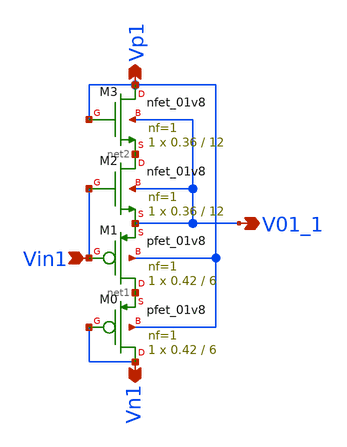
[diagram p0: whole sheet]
** sch_path: xschem/Vth_sch/Symbol/th01_1.sch
**.subckt th01_1 Vn1 Vp1 Vin1 V01_1
*.opin Vn1
*.opin Vp1
*.ipin Vin1
*.opin V01_1
XM0 Vn1 Vn1 net1 Vp1 sky130_fd_pr__pfet_01v8 L=6 W=0.42 nf=1 ad='int((nf+1)/2) * W/nf * 0.29' as='int((nf+2)/2) * W/nf * 0.29'
+ pd='2*int((nf+1)/2) * (W/nf + 0.29)' ps='2*int((nf+2)/2) * (W/nf + 0.29)' nrd='0.29 / W' nrs='0.29 / W'
+ sa=0 sb=0 sd=0 mult=1 m=1
XM3 Vp1 Vp1 net2 V01_1 sky130_fd_pr__nfet_01v8 L=12 W=0.36 nf=1 ad='int((nf+1)/2) * W/nf * 0.29' as='int((nf+2)/2) * W/nf * 0.29'
+ pd='2*int((nf+1)/2) * (W/nf + 0.29)' ps='2*int((nf+2)/2) * (W/nf + 0.29)' nrd='0.29 / W' nrs='0.29 / W'
+ sa=0 sb=0 sd=0 mult=1 m=1
XM1 net1 Vin1 V01_1 Vp1 sky130_fd_pr__pfet_01v8 L=6 W=0.42 nf=1 ad='int((nf+1)/2) * W/nf * 0.29' as='int((nf+2)/2) * W/nf * 0.29'
+ pd='2*int((nf+1)/2) * (W/nf + 0.29)' ps='2*int((nf+2)/2) * (W/nf + 0.29)' nrd='0.29 / W' nrs='0.29 / W'
+ sa=0 sb=0 sd=0 mult=1 m=1
XM2 net2 Vin1 V01_1 V01_1 sky130_fd_pr__nfet_01v8 L=12 W=0.36 nf=1 ad='int((nf+1)/2) * W/nf * 0.29' as='int((nf+2)/2) * W/nf * 0.29'
+ pd='2*int((nf+1)/2) * (W/nf + 0.29)' ps='2*int((nf+2)/2) * (W/nf + 0.29)' nrd='0.29 / W' nrs='0.29 / W'
+ sa=0 sb=0 sd=0 mult=1 m=1
**.ends
.end
